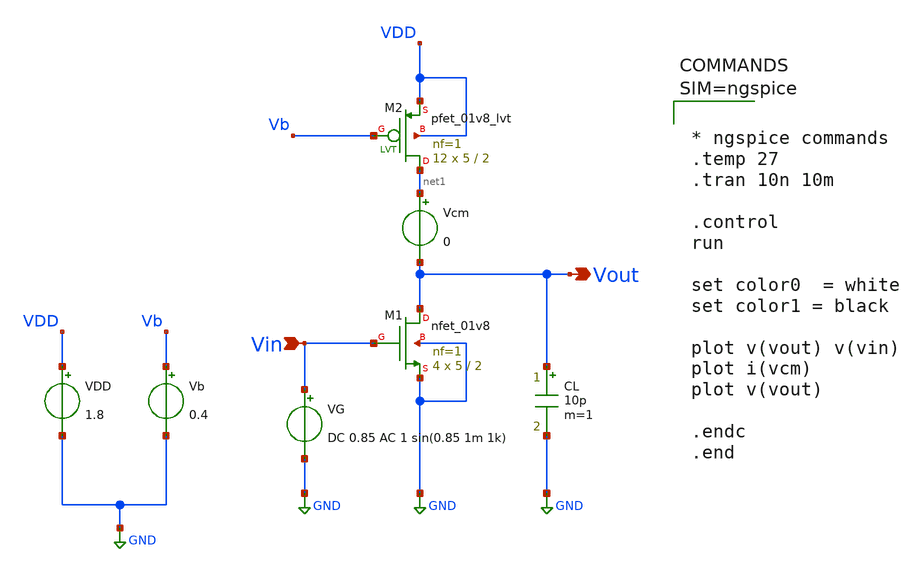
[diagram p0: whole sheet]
** sch_path: Common_Source_PMOS_Load_ckts/CS_Amp_PMOS_Triode_Load_Ckts/CS_Amp_PMOS_Triode_Load_AC_Transient_Analysis.sch
**.subckt CS_Amp_PMOS_Triode_Load_AC_Transient_Analysis Vin Vout
*.ipin Vin
*.opin Vout
XM1 Vout Vin GND GND sky130_fd_pr__nfet_01v8 L=2 W=5 nf=1 ad='int((1 + 1)/2) * 5 / 1 * 0.29' as='int((1 + 2)/2) * 5 / 1 * 0.29'
+ pd='2*int((1 + 1)/2) * (5 / 1 + 0.29)' ps='2*int((1 + 2)/2) * (5 / 1 + 0.29)' nrd='0.29 / 5 ' nrs='0.29 / 5 '
+ sa=0 sb=0 sd=0 mult=4 m=4
XM2 net1 Vb VDD VDD sky130_fd_pr__pfet_01v8_lvt L=2 W=5 nf=1 ad='int((1 + 1)/2) * 5 / 1 * 0.29' as='int((1 + 2)/2) * 5 / 1 * 0.29'
+ pd='2*int((1 + 1)/2) * (5 / 1 + 0.29)' ps='2*int((1 + 2)/2) * (5 / 1 + 0.29)' nrd='0.29 / 5 ' nrs='0.29 / 5 '
+ sa=0 sb=0 sd=0 mult=12 m=12
Vcm net1 Vout 0
VG Vin GND DC 0.85 AC 1 sin(0.85 1m 1k)
Vb Vb GND 0.4
VDD VDD GND 1.8
CL Vout GND 10p m=1
**** begin user architecture code



* ngspice commands
.temp 27
.tran 10n 10m

.control
run

set color0  = white
set color1 = black

plot v(vout) v(vin)
plot i(vcm)
plot v(vout)

.endc
.end





** opencircuitdesign pdks install
.lib $::SKYWATER_MODELS/sky130.lib.spice tt

**** end user architecture code
**.ends
.GLOBAL GND
.end
